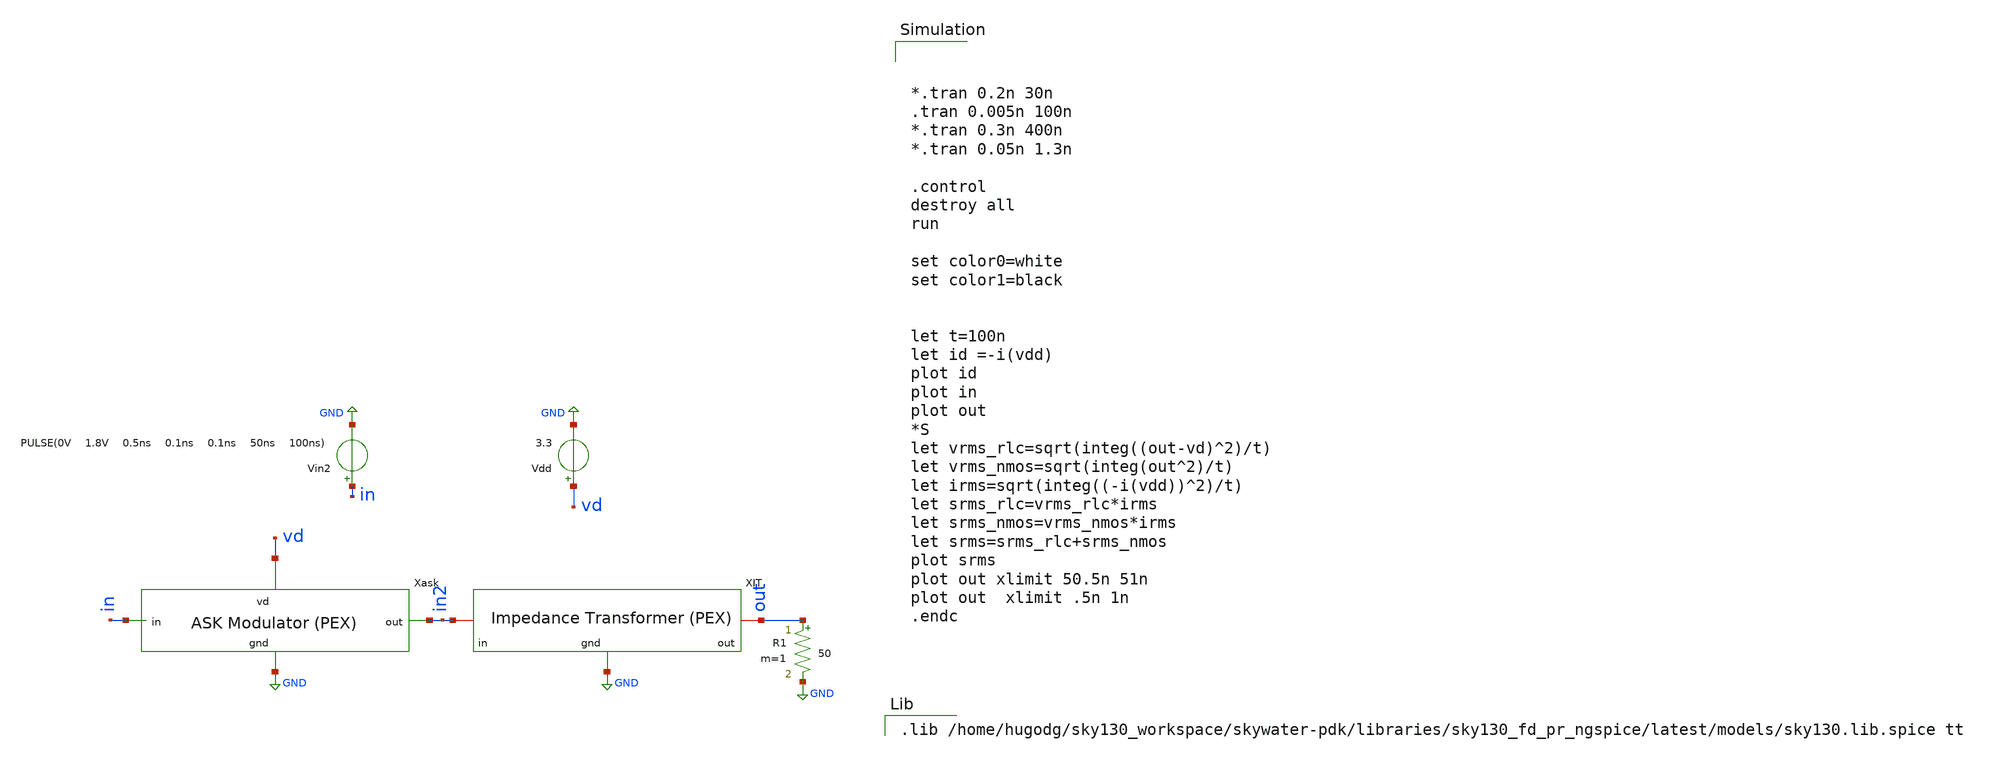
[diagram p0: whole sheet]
** sch_path: impedance-transformer/xschem/impedance-transformer-pex_tb-tran.sch
**.subckt impedance-transformer-pex_tb-tran
Vdd vd GND 3.3
Vin2 in GND PULSE(0V 1.8V 0.5ns 0.1ns 0.1ns 50ns 100ns)
x1 vd in2 in GND ask-modulator-pex
x2 in2 out GND impedance-transformer-pex
R1 out GND 50 m=1
**** begin user architecture code



*.tran 0.2n 30n
.tran 0.005n 100n
*.tran 0.3n 400n
*.tran 0.05n 1.3n

.control
destroy all
run

set color0=white
set color1=black


let t=100n
let id =-i(vdd)
plot id
plot in
plot out
*S
let vrms_rlc=sqrt(integ((out-vd)^2)/t)
let vrms_nmos=sqrt(integ(out^2)/t)
let irms=sqrt(integ((-i(vdd))^2)/t)
let srms_rlc=vrms_rlc*irms
let srms_nmos=vrms_nmos*irms
let srms=srms_rlc+srms_nmos
plot srms
plot out xlimit 50.5n 51n
plot out  xlimit .5n 1n
.endc


.lib /home/hugodg/sky130_workspace/skywater-pdk/libraries/sky130_fd_pr_ngspice/latest/models/sky130.lib.spice tt

**** end user architecture code
**.ends
.GLOBAL GND
.end
